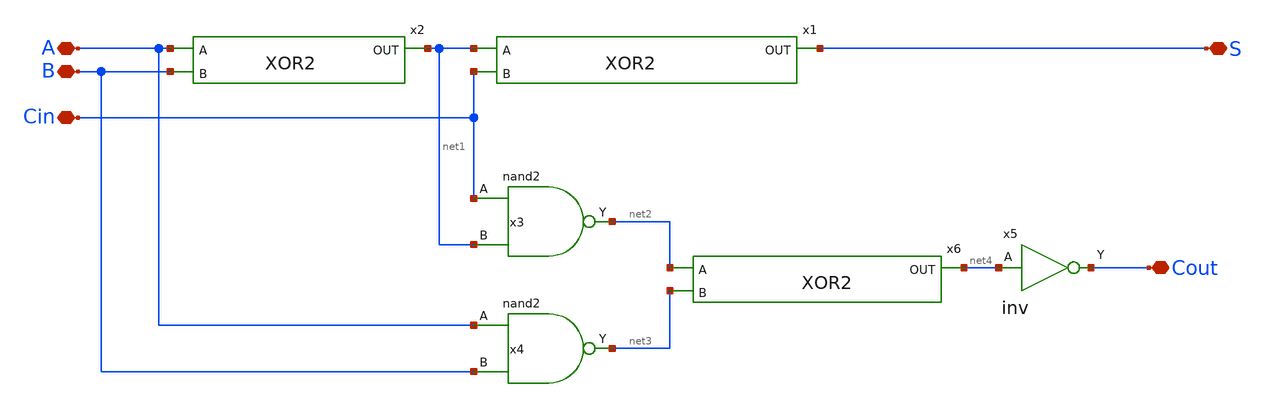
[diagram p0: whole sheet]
** sch_path: design/xschem/ADDER/full_adder.sch
**.subckt full_adder A B Cin S Cout
*.iopin A
*.iopin B
*.iopin Cin
*.iopin S
*.iopin Cout
x2 A B net1 XOR2
x1 net1 Cin S XOR2
x3 Cin net1 VSS VDD net2 nand2
x4 A B VSS VDD net3 nand2
x6 net2 net3 net4 XOR2
x5 net4 VSS VDD Cout inv
**.ends
.end
